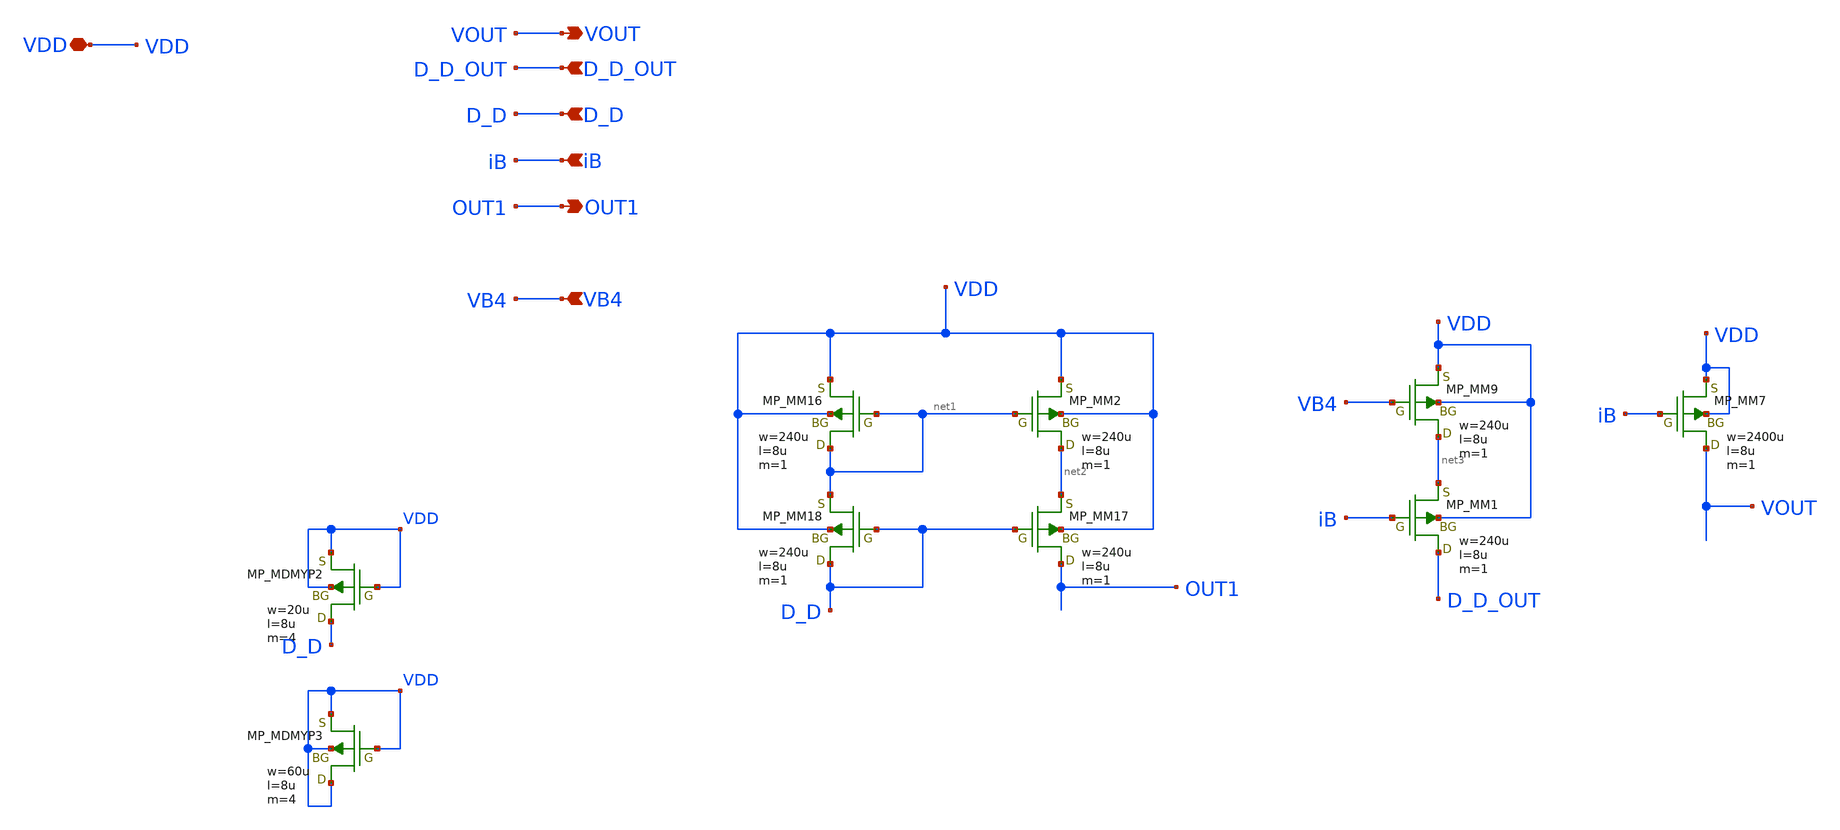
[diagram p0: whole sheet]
** sch_path: member_project/AM_Radio/noritsuna/xschem/DIFF_PMOS.sch
**.subckt DIFF_PMOS VDD OUT1 D_D VB4 D_D_OUT VOUT iB
*.iopin VDD
*.opin OUT1
*.ipin D_D
*.ipin VB4
*.ipin D_D_OUT
*.opin VOUT
*.ipin iB
MM2 net2 net1 VDD VDD PMOS w=240u l=8u as=0 ad=0 ps=0 pd=0 nrd=0 nrs=0 m=1
MM16 net1 net1 VDD VDD PMOS w=240u l=8u as=0 ad=0 ps=0 pd=0 nrd=0 nrs=0 m=1
MM17 OUT1 D_D net2 VDD PMOS w=240u l=8u as=0 ad=0 ps=0 pd=0 nrd=0 nrs=0 m=1
MM18 D_D D_D net1 VDD PMOS w=240u l=8u as=0 ad=0 ps=0 pd=0 nrd=0 nrs=0 m=1
MM1 D_D_OUT iB net3 VDD PMOS w=240u l=8u as=0 ad=0 ps=0 pd=0 nrd=0 nrs=0 m=1
MM9 net3 VB4 VDD VDD PMOS w=240u l=8u as=0 ad=0 ps=0 pd=0 nrd=0 nrs=0 m=1
MM7 VOUT iB VDD VDD PMOS w=2400u l=8u as=0 ad=0 ps=0 pd=0 nrd=0 nrs=0 m=1
XMDMYP2 D_D VDD VDD VDD PMOS w=20u l=8u as=0 ad=0 ps=0 pd=0 nrd=0 nrs=0 m=4
XMDMYP3 VDD VDD VDD VDD PMOS w=60u l=8u as=0 ad=0 ps=0 pd=0 nrd=0 nrs=0 m=4
**.ends
.end
